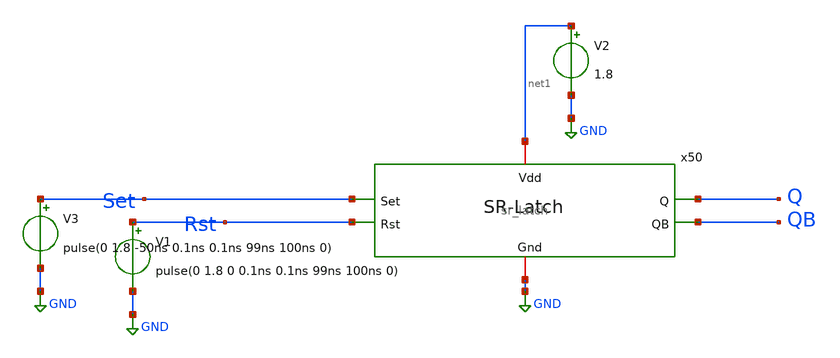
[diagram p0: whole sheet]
** sch_path: xschem/sr_latch_tb.sch
**.subckt sr_latch_tb
x1 net1 Set Rst Q QB GND sr_latch
V1 Rst GND pulse(0 1.8 0 0.1ns 0.1ns 99ns 100ns 0)
V3 Set GND pulse(0 1.8 -50ns 0.1ns 0.1ns 99ns 100ns 0)
V2 net1 GND 1.8
**** begin user architecture code


* .include /home/lbraga/Projects/relax_oscillator/mag/sr_latch.spice
.lib /usr/local/share/pdk/sky130A/libs.tech/ngspice/sky130.lib.spice tt

.control
        tran 0.1n .2us
	set color0=rgb:f/f/f
	set xbrushwidth=3
        plot v(Set) v(Rst)
	options color3=green
	options color2=orange
	plot v(Q) v(QB)
.endc
.save all


**** end user architecture code
**.ends
.GLOBAL GND
.end
